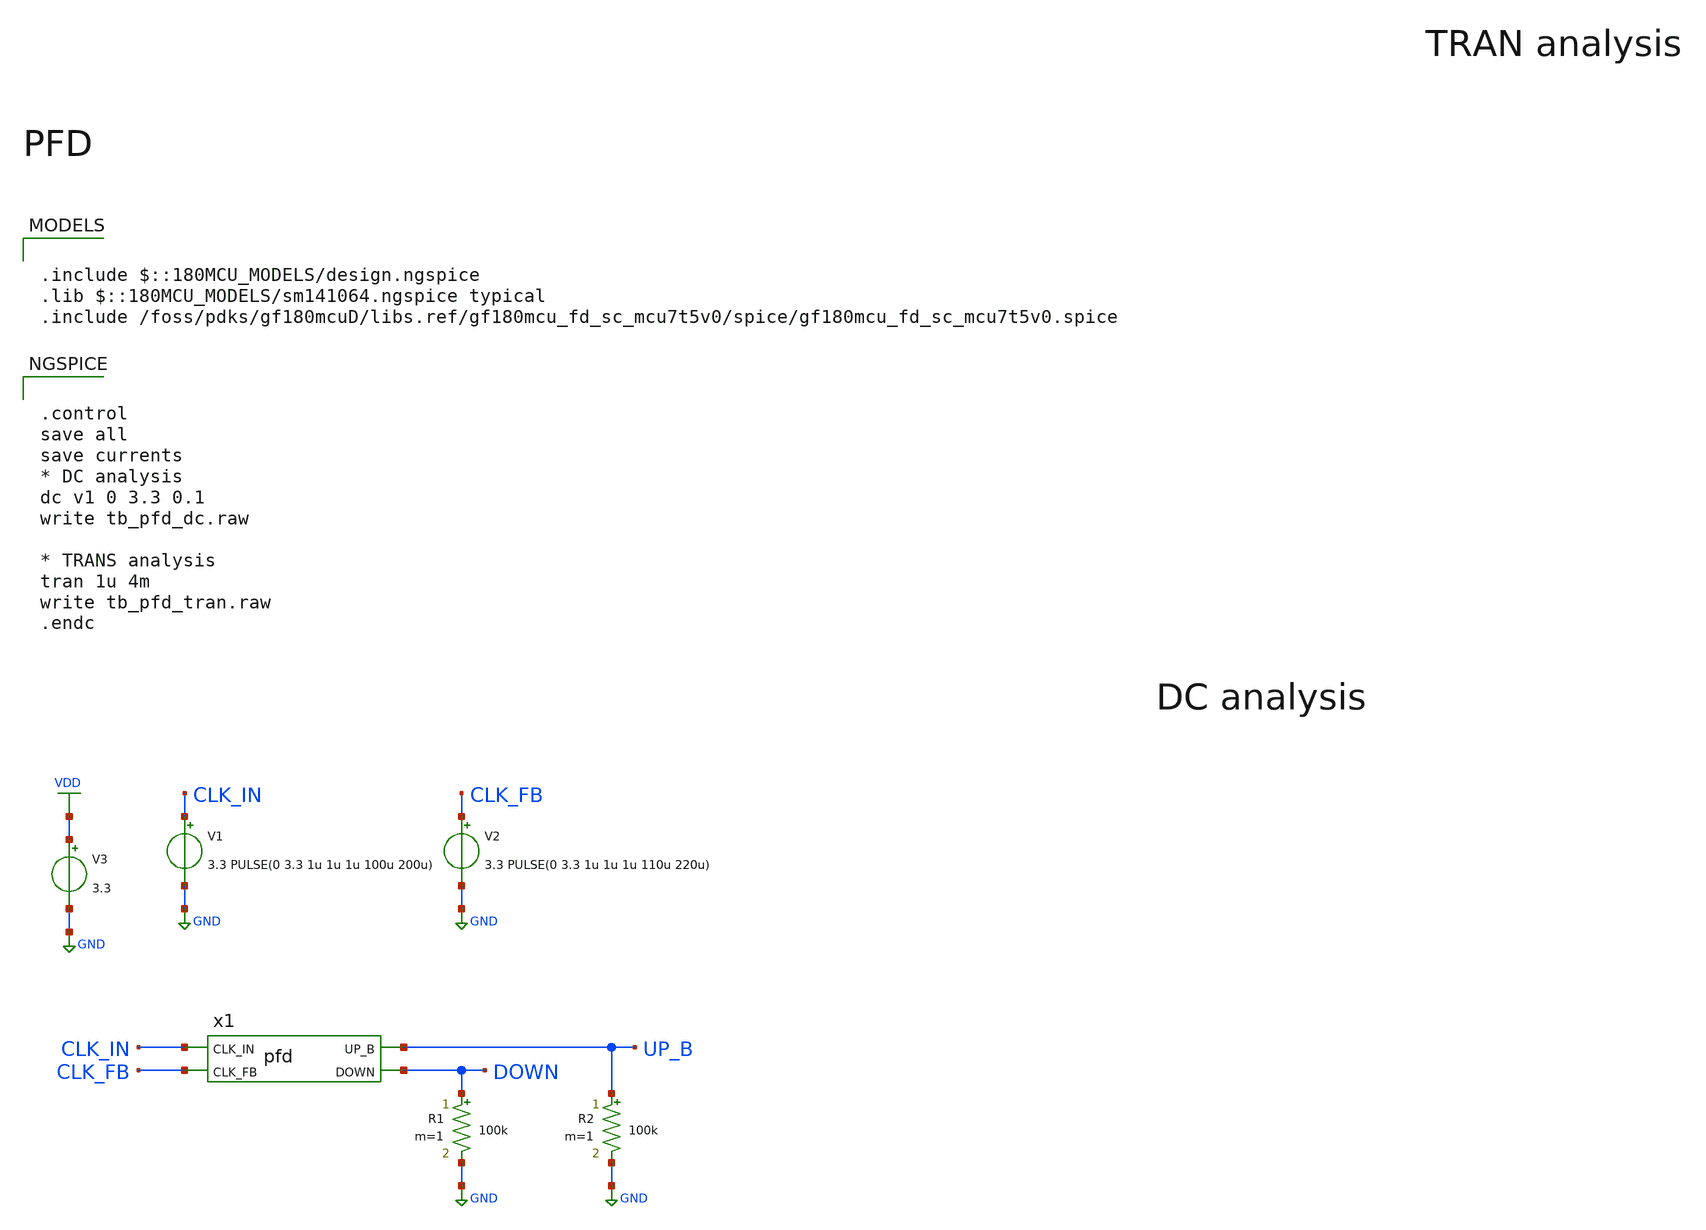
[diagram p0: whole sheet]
** sch_path: designs/libs/tb_analog/tb_pfd/tb_pfd.sch
* Copyright 2022 GlobalFoundries PDK Authors
* Licensed under the Apache License, Version 2.0 (the "License");
* you may not use this file except in compliance with the License.
* You may obtain a copy of the License at
* https://www.apache.org/licenses/LICENSE-2.0
* Unless required by applicable law or agreed to in writing, software
* distributed under the License is distributed on an "AS IS" BASIS,
* WITHOUT WARRANTIES OR CONDITIONS OF ANY KIND, either express or implied.
* See the License for the specific language governing permissions and
* limitations under the License.
**.subckt tb_pfd
V1 CLK_IN GND 3.3 PULSE(0 3.3 1u 1u 1u 100u 200u)
R1 DOWN GND 100k m=1
x1 UP_B CLK_IN CLK_FB DOWN pfd
R2 UP_B GND 100k m=1
V2 CLK_FB GND 3.3 PULSE(0 3.3 1u 1u 1u 110u 220u)
V3 VDD GND 3.3
**** begin user architecture code

.include $::180MCU_MODELS/design.ngspice
.lib $::180MCU_MODELS/sm141064.ngspice typical
.include /foss/pdks/gf180mcuD/libs.ref/gf180mcu_fd_sc_mcu7t5v0/spice/gf180mcu_fd_sc_mcu7t5v0.spice




.control
save all
save currents
* DC analysis
dc v1 0 3.3 0.1
write tb_pfd_dc.raw

* TRANS analysis
tran 1u 4m
write tb_pfd_tran.raw
.endc


**** end user architecture code
**.ends

* expanding   symbol:  libs/core_analog/pfd/pfd.sym # of pins=4
** sym_path: designs/libs/core_analog/pfd/pfd.sym
** sch_path: designs/libs/core_analog/pfd/pfd.sch
.subckt pfd UP_B CLK_IN CLK_FB DOWN
*.opin UP_B
*.opin DOWN
*.ipin CLK_IN
*.ipin CLK_FB
x1 VDD net2 CLK_IN net1 VDD VDD GND GND gf180mcu_fd_sc_mcu7t5v0__dffrnq_1
x2 VDD net2 CLK_FB DOWN VDD VDD GND GND gf180mcu_fd_sc_mcu7t5v0__dffrnq_1
x3 net1 DOWN net2 VDD VDD GND GND gf180mcu_fd_sc_mcu7t5v0__nand2_1
x4 net1 UP_B VDD VDD GND GND gf180mcu_fd_sc_mcu7t5v0__inv_1
.ends

.GLOBAL GND
.GLOBAL VDD
.end
